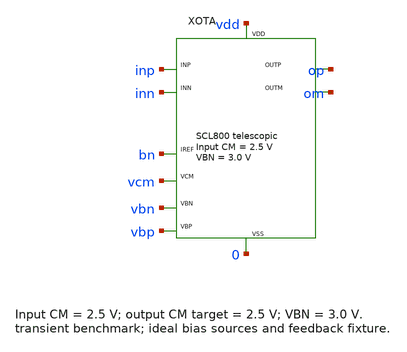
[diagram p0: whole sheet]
** sch_path: OTA/final_design/designs/ota_cm2p5_transient_tb.sch
**.subckt ota_cm2p5_transient_tb
XOTA inp inn op om vdd 0 bn vcm vbn vbp ota_telescopic_cm2p5
**** begin user architecture code

.include ../models/scl08_models.inc
.include ../models/ota_cm2p5_C.spice
.temp 27
.options reltol=1e-5 vntol=1e-8 abstol=1e-12 numdgt=12 method=gear maxord=2
VDD vdd 0 5
IREF vdd bn 3.5u
VCM vcm 0 2.5
VBN vbn 0 3
VBP vbp vdd -2.2
CLP op 0 5p
CLM om 0 5p
EOD od 0 op om 1
VICM icm 0 2.5
EIP inp icm cmd od 0.5
EIM inn icm od cmd 0.5
VCMD cmd 0 PWL(0 -1 10u -1 10.01u 1 30u 1 30.01u -1 50u -1)
.control
set wr_singlescale
set wr_vecnames
op
print v(op) v(om) i(vdd)
tran 10n 50u
wrdata transient.dat v(op) v(om) v(inp) v(inn) i(vdd) v(cmd)
write ota_cm2p5_transient.raw v(op) v(om) v(inp) v(inn) v(cmd)
quit
.endc

**** end user architecture code
**.ends
.end
